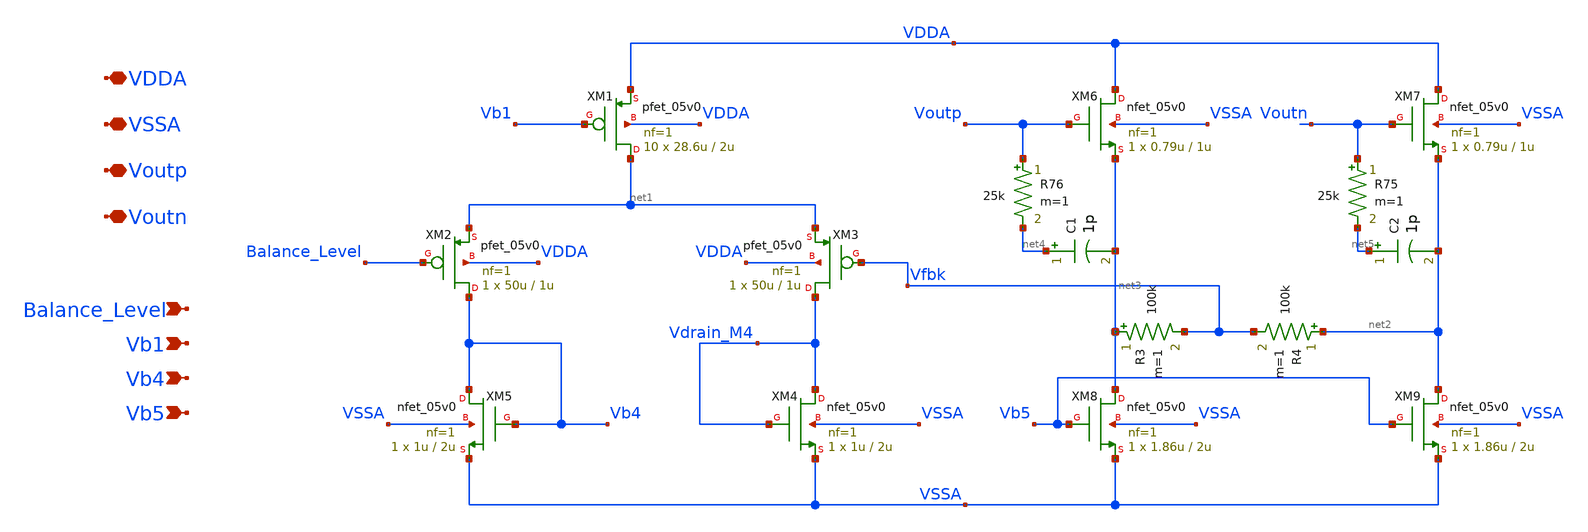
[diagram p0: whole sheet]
** sch_path: schematic/cmfb.sch
**.subckt cmfb VDDA VSSA Vb4 Balance_Level Vb1 Vb5 Voutp Voutn
*.iopin VDDA
*.iopin VSSA
*.ipin Vb4
*.ipin Balance_Level
*.ipin Vb1
*.ipin Vb5
*.iopin Voutp
*.iopin Voutn
XM1 net1 Vb1 VDDA VDDA pfet_05v0 L=2u W=28.6u nf=1 ad='int((nf+1)/2) * W/nf * 0.18u' as='int((nf+2)/2) * W/nf * 0.18u'
+ pd='2*int((nf+1)/2) * (W/nf + 0.18u)' ps='2*int((nf+2)/2) * (W/nf + 0.18u)' nrd='0.18u / W' nrs='0.18u / W'
+ sa=0 sb=0 sd=0 m=10
XM2 Vb4 Balance_Level net1 VDDA pfet_05v0 L=1u W=50u nf=1 ad='int((nf+1)/2) * W/nf * 0.18u' as='int((nf+2)/2) * W/nf * 0.18u'
+ pd='2*int((nf+1)/2) * (W/nf + 0.18u)' ps='2*int((nf+2)/2) * (W/nf + 0.18u)' nrd='0.18u / W' nrs='0.18u / W'
+ sa=0 sb=0 sd=0 m=1
XM3 Vdrain_M4 Vfbk net1 VDDA pfet_05v0 L=1u W=50u nf=1 ad='int((nf+1)/2) * W/nf * 0.18u' as='int((nf+2)/2) * W/nf * 0.18u'
+ pd='2*int((nf+1)/2) * (W/nf + 0.18u)' ps='2*int((nf+2)/2) * (W/nf + 0.18u)' nrd='0.18u / W' nrs='0.18u / W'
+ sa=0 sb=0 sd=0 m=1
XM4 Vdrain_M4 Vdrain_M4 VSSA VSSA nfet_05v0 L=2u W=1u nf=1 ad='int((nf+1)/2) * W/nf * 0.18u' as='int((nf+2)/2) * W/nf * 0.18u'
+ pd='2*int((nf+1)/2) * (W/nf + 0.18u)' ps='2*int((nf+2)/2) * (W/nf + 0.18u)' nrd='0.18u / W' nrs='0.18u / W'
+ sa=0 sb=0 sd=0 m=1
XM5 Vb4 Vb4 VSSA VSSA nfet_05v0 L=2u W=1u nf=1 ad='int((nf+1)/2) * W/nf * 0.18u' as='int((nf+2)/2) * W/nf * 0.18u'
+ pd='2*int((nf+1)/2) * (W/nf + 0.18u)' ps='2*int((nf+2)/2) * (W/nf + 0.18u)' nrd='0.18u / W' nrs='0.18u / W'
+ sa=0 sb=0 sd=0 m=1
XM6 VDDA Voutp net3 VSSA nfet_05v0 L=1u W=0.79u nf=1 ad='int((nf+1)/2) * W/nf * 0.18u' as='int((nf+2)/2) * W/nf * 0.18u'
+ pd='2*int((nf+1)/2) * (W/nf + 0.18u)' ps='2*int((nf+2)/2) * (W/nf + 0.18u)' nrd='0.18u / W' nrs='0.18u / W'
+ sa=0 sb=0 sd=0 m=1
XM7 VDDA Voutn net2 VSSA nfet_05v0 L=1u W=0.79u nf=1 ad='int((nf+1)/2) * W/nf * 0.18u' as='int((nf+2)/2) * W/nf * 0.18u'
+ pd='2*int((nf+1)/2) * (W/nf + 0.18u)' ps='2*int((nf+2)/2) * (W/nf + 0.18u)' nrd='0.18u / W' nrs='0.18u / W'
+ sa=0 sb=0 sd=0 m=1
R3 net3 Vfbk 100k m=1
R4 net2 Vfbk 100k m=1
XM8 net3 Vb5 VSSA VSSA nfet_05v0 L=2u W=1.86u nf=1 ad='int((nf+1)/2) * W/nf * 0.18u' as='int((nf+2)/2) * W/nf * 0.18u'
+ pd='2*int((nf+1)/2) * (W/nf + 0.18u)' ps='2*int((nf+2)/2) * (W/nf + 0.18u)' nrd='0.18u / W' nrs='0.18u / W'
+ sa=0 sb=0 sd=0 m=1
XM9 net2 Vb5 VSSA VSSA nfet_05v0 L=2u W=1.86u nf=1 ad='int((nf+1)/2) * W/nf * 0.18u' as='int((nf+2)/2) * W/nf * 0.18u'
+ pd='2*int((nf+1)/2) * (W/nf + 0.18u)' ps='2*int((nf+2)/2) * (W/nf + 0.18u)' nrd='0.18u / W' nrs='0.18u / W'
+ sa=0 sb=0 sd=0 m=1
R75 Voutn net5 25k m=1
R76 Voutp net4 25k m=1
C1 net4 net3 1p m=1
C2 net5 net2 1p m=1
**.ends
.end
